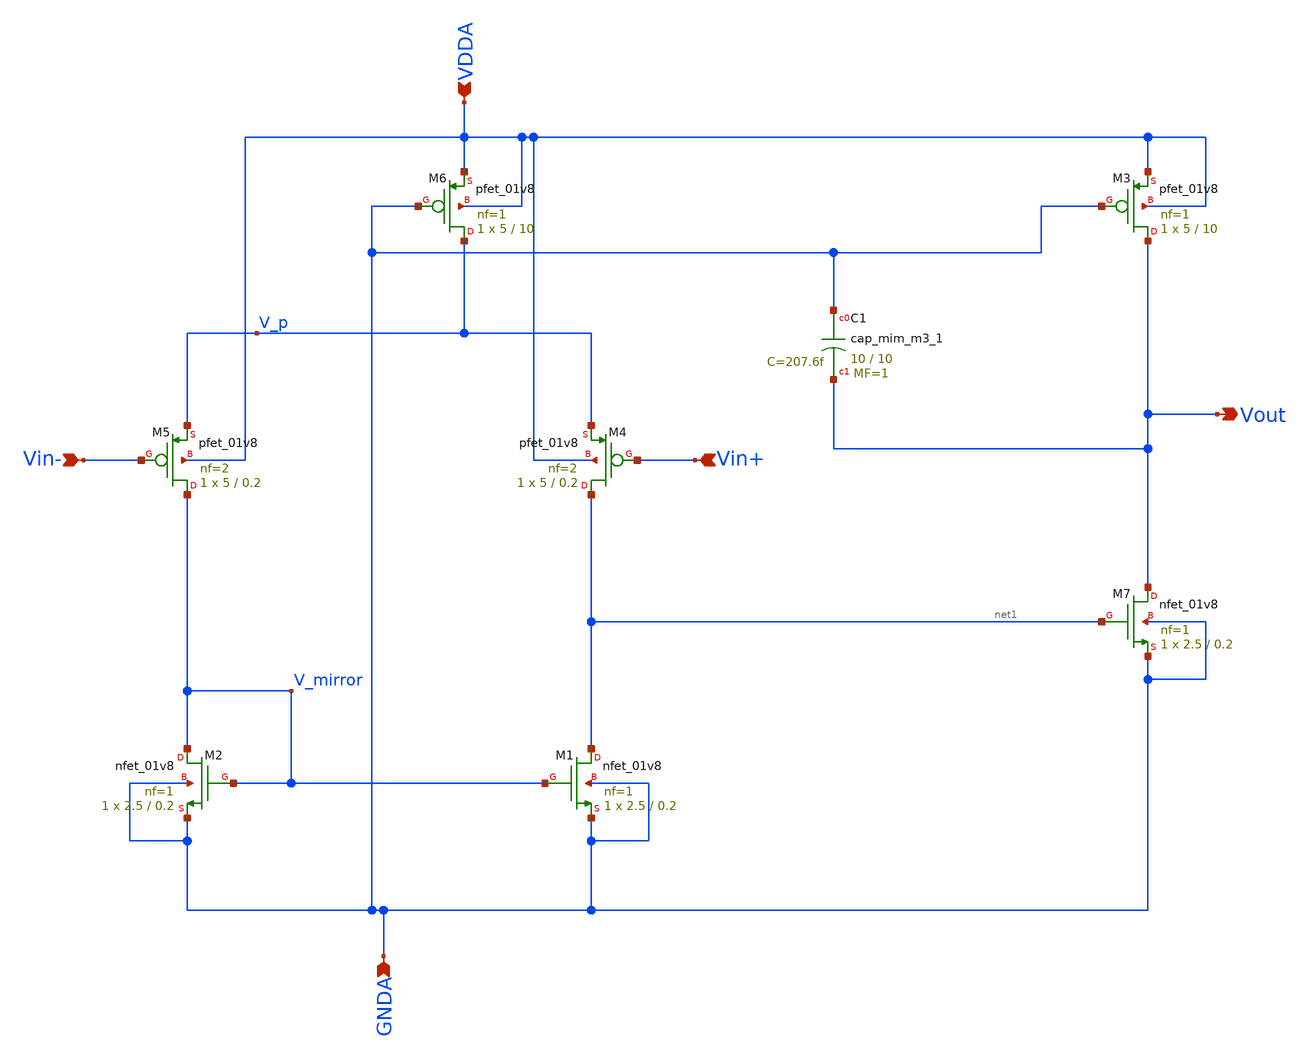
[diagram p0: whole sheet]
** sch_path: projects/bandgapref/xschem_ngspice/new_files/opamp_bandgap_3.sch
**.subckt opamp_bandgap_3 Vin+ Vout Vin- GNDA VDDA
*.ipin Vin+
*.opin Vout
*.ipin Vin-
*.ipin GNDA
*.ipin VDDA
XM1 net1 V_mirror GNDA GNDA sky130_fd_pr__nfet_01v8 L=0.2 W=2.5 nf=1 ad='int((nf+1)/2) * W/nf * 0.29'
+ as='int((nf+2)/2) * W/nf * 0.29' pd='2*int((nf+1)/2) * (W/nf + 0.29)' ps='2*int((nf+2)/2) * (W/nf + 0.29)'
+ nrd='0.29 / W' nrs='0.29 / W' sa=0 sb=0 sd=0 mult=1 m=1
XM2 V_mirror V_mirror GNDA GNDA sky130_fd_pr__nfet_01v8 L=0.2 W=2.5 nf=1 ad='int((nf+1)/2) * W/nf * 0.29'
+ as='int((nf+2)/2) * W/nf * 0.29' pd='2*int((nf+1)/2) * (W/nf + 0.29)' ps='2*int((nf+2)/2) * (W/nf + 0.29)'
+ nrd='0.29 / W' nrs='0.29 / W' sa=0 sb=0 sd=0 mult=1 m=1
XM4 net1 Vin+ V_p VDDA sky130_fd_pr__pfet_01v8 L=0.2 W=5 nf=2 ad='int((nf+1)/2) * W/nf * 0.29' as='int((nf+2)/2) * W/nf * 0.29'
+ pd='2*int((nf+1)/2) * (W/nf + 0.29)' ps='2*int((nf+2)/2) * (W/nf + 0.29)' nrd='0.29 / W' nrs='0.29 / W'
+ sa=0 sb=0 sd=0 mult=1 m=1
XM5 V_mirror Vin- V_p VDDA sky130_fd_pr__pfet_01v8 L=0.2 W=5 nf=2 ad='int((nf+1)/2) * W/nf * 0.29' as='int((nf+2)/2) * W/nf * 0.29'
+ pd='2*int((nf+1)/2) * (W/nf + 0.29)' ps='2*int((nf+2)/2) * (W/nf + 0.29)' nrd='0.29 / W' nrs='0.29 / W'
+ sa=0 sb=0 sd=0 mult=1 m=1
XM6 V_p GNDA VDDA VDDA sky130_fd_pr__pfet_01v8 L=10 W=5 nf=1 ad='int((nf+1)/2) * W/nf * 0.29' as='int((nf+2)/2) * W/nf * 0.29'
+ pd='2*int((nf+1)/2) * (W/nf + 0.29)' ps='2*int((nf+2)/2) * (W/nf + 0.29)' nrd='0.29 / W' nrs='0.29 / W'
+ sa=0 sb=0 sd=0 mult=1 m=1
XM3 Vout GNDA VDDA VDDA sky130_fd_pr__pfet_01v8 L=10 W=5 nf=1 ad='int((nf+1)/2) * W/nf * 0.29' as='int((nf+2)/2) * W/nf * 0.29'
+ pd='2*int((nf+1)/2) * (W/nf + 0.29)' ps='2*int((nf+2)/2) * (W/nf + 0.29)' nrd='0.29 / W' nrs='0.29 / W'
+ sa=0 sb=0 sd=0 mult=1 m=1
XM7 Vout net1 GNDA GNDA sky130_fd_pr__nfet_01v8 L=0.2 W=2.5 nf=1 ad='int((nf+1)/2) * W/nf * 0.29' as='int((nf+2)/2) * W/nf * 0.29'
+ pd='2*int((nf+1)/2) * (W/nf + 0.29)' ps='2*int((nf+2)/2) * (W/nf + 0.29)' nrd='0.29 / W' nrs='0.29 / W'
+ sa=0 sb=0 sd=0 mult=1 m=1
XC1 GNDA Vout sky130_fd_pr__cap_mim_m3_1 W=10 L=10 MF=1 m=1
**.ends
.end
